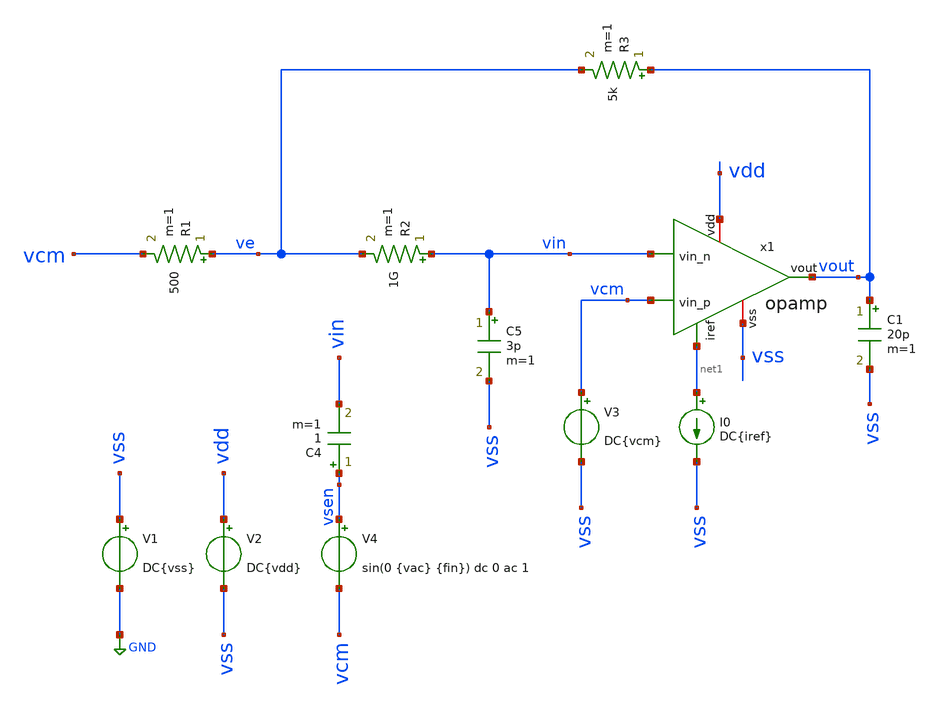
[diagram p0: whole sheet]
** sch_path: tb_opamp_openloop.sch
**.subckt tb_opamp_openloop
V1 vss GND DC{vss}
V2 vdd vss DC{vdd}
V3 vcm vss DC{vcm}
V4 vsen vcm sin(0 {vac} {fin}) dc 0 ac 1
C4 vsen vin 1 m=1
I0 net1 vss DC{iref}
R1 ve vcm 500 m=1
R2 vin ve 1G m=1
R3 vout ve 5k m=1
C5 vin vss 3p m=1
C1 vout vss 20p m=1
x1 vdd net1 vin vcm vout vss opamp
**** begin user architecture code




* Circuit Parameters

.param w_mirror_1 = 65
.param l_mirror_1 = 0.6
.param m_mirror_1 = 10

.param w_par = 41
.param l_par = 0.49
.param m_par = 48

.param w_mirror_2 = 40
.param l_mirror_2 = 1.4
.param m_mirror_2 = 8
.param cc = 13.25p

.param branch_2 = 20

.param iref = 100u
.param vdd  = 1.8
.param vss  = 0.0
.param vcm  = 0.8
.param vac  = 60m
.param fin  = 9.765625e5
.options TEMP = 65

* Include Models
.lib ~/skywater/skywater-pdk/libraries/sky130_fd_pr_ngspice/latest/models/corners/sky130.lib TT

* OP Parameters & Singals to save
.save all  @M.X1.XM1.msky130_fd_pr__pfet_01v8_lvt[id] @M.X1.XM1.msky130_fd_pr__pfet_01v8_lvt[vth] @M.X1.XM1.msky130_fd_pr__pfet_01v8_lvt[vgs] @M.X1.XM1.msky130_fd_pr__pfet_01v8_lvt[vds] @M.X1.XM1.msky130_fd_pr__pfet_01v8_lvt[vdsat] @M.X1.XM1.msky130_fd_pr__pfet_01v8_lvt[gm] @M.X1.XM1.msky130_fd_pr__pfet_01v8_lvt[gds]  @M.X1.XM2.msky130_fd_pr__pfet_01v8_lvt[id] @M.X1.XM2.msky130_fd_pr__pfet_01v8_lvt[vth] @M.X1.XM2.msky130_fd_pr__pfet_01v8_lvt[vgs] @M.X1.XM2.msky130_fd_pr__pfet_01v8_lvt[vds] @M.X1.XM2.msky130_fd_pr__pfet_01v8_lvt[vdsat] @M.X1.XM2.msky130_fd_pr__pfet_01v8_lvt[gm] @M.X1.XM2.msky130_fd_pr__pfet_01v8_lvt[gds] @M.X1.XM2.msky130_fd_pr__pfet_01v8[cgg]  @M.X1.XM3.msky130_fd_pr__nfet_01v8[id] @M.X1.XM3.msky130_fd_pr__nfet_01v8[vth] @M.X1.XM3.msky130_fd_pr__nfet_01v8[vgs] @M.X1.XM3.msky130_fd_pr__nfet_01v8[vds] @M.X1.XM3.msky130_fd_pr__nfet_01v8[vdsat] @M.X1.XM3.msky130_fd_pr__nfet_01v8[gm] @M.X1.XM3.msky130_fd_pr__nfet_01v8[gds]  @M.X1.XM4.msky130_fd_pr__nfet_01v8[id] @M.X1.XM4.msky130_fd_pr__nfet_01v8[vth] @M.X1.XM4.msky130_fd_pr__nfet_01v8[vgs] @M.X1.XM4.msky130_fd_pr__nfet_01v8[vds] @M.X1.XM4.msky130_fd_pr__nfet_01v8[vdsat] @M.X1.XM4.msky130_fd_pr__nfet_01v8[gm] @M.X1.XM4.msky130_fd_pr__nfet_01v8[gds]  @M.X1.XM5.msky130_fd_pr__pfet_01v8[id] @M.X1.XM5.msky130_fd_pr__pfet_01v8[vth] @M.X1.XM5.msky130_fd_pr__pfet_01v8[vgs] @M.X1.XM5.msky130_fd_pr__pfet_01v8[vds] @M.X1.XM5.msky130_fd_pr__pfet_01v8[vdsat] @M.X1.XM5.msky130_fd_pr__pfet_01v8[gm] @M.X1.XM5.msky130_fd_pr__pfet_01v8[gds]  @M.X1.XM6.msky130_fd_pr__nfet_01v8[id] @M.X1.XM6.msky130_fd_pr__nfet_01v8[vth] @M.X1.XM6.msky130_fd_pr__nfet_01v8[vgs] @M.X1.XM6.msky130_fd_pr__nfet_01v8[vds] @M.X1.XM6.msky130_fd_pr__nfet_01v8[vdsat] @M.X1.XM6.msky130_fd_pr__nfet_01v8[gm] @M.X1.XM6.msky130_fd_pr__nfet_01v8[gds] @M.X1.XM6.msky130_fd_pr__nfet_01v8[cgs]  @M.X1.XM7.msky130_fd_pr__pfet_01v8[id] @M.X1.XM7.msky130_fd_pr__pfet_01v8[vth] @M.X1.XM7.msky130_fd_pr__pfet_01v8[vgs] @M.X1.XM7.msky130_fd_pr__pfet_01v8[vds] @M.X1.XM7.msky130_fd_pr__pfet_01v8[vdsat] @M.X1.XM7.msky130_fd_pr__pfet_01v8[gm] @M.X1.XM7.msky130_fd_pr__pfet_01v8[gds]  @M.X1.XM8.msky130_fd_pr__pfet_01v8[id] @M.X1.XM8.msky130_fd_pr__pfet_01v8[vth] @M.X1.XM8.msky130_fd_pr__pfet_01v8[vgs] @M.X1.XM8.msky130_fd_pr__pfet_01v8[vds] @M.X1.XM8.msky130_fd_pr__pfet_01v8[vdsat] @M.X1.XM8.msky130_fd_pr__pfet_01v8[gm] @M.X1.XM8.msky130_fd_pr__pfet_01v8[gds]  @M.X1.XM9.msky130_fd_pr__nfet_01v8[id] @M.X1.XM9.msky130_fd_pr__nfet_01v8[vth] @M.X1.XM9.msky130_fd_pr__nfet_01v8[vgs] @M.X1.XM9.msky130_fd_pr__nfet_01v8[vds] @M.X1.XM9.msky130_fd_pr__nfet_01v8[vdsat] @M.X1.XM9.msky130_fd_pr__nfet_01v8[gm] @M.X1.XM9.msky130_fd_pr__nfet_01v8[gds]

*Simulation
.control
  set color0 = white

  ac dec 100 1 10G
  setplot ac1
  meas ac GBW when vdb(vout)=0
  meas ac DCG find vdb(vout) at=1
  meas ac PM find vp(vout) when vdb(vout)=0
  print PM*180/PI
  meas ac GM find vdb(vout) when vp(vout)=0
  plot vdb(vout) {vp(vout)*180/PI}
  write tb_opamp_openloop_ac1.raw

  reset
  op
  setplot op1
  unset filetype
  write tb_opamp_openloop.raw
.endc

.end


**** end user architecture code
**.ends

* expanding   symbol:  opamp.sym # of pins=6
** sym_path: opamp.sym
** sch_path: opamp.sch
.subckt opamp vdd iref vin_n vin_p vout vss
*.iopin vdd
*.iopin vss
*.ipin vin_n
*.ipin vin_p
*.ipin iref
*.opin vout
XM3 vbn vbn vss vss sky130_fd_pr__nfet_01v8 L={l_mirror_2} W={w_mirror_2} nf=1 ad='W * 0.29' as='W * 0.29'
+ pd='2 * (W + 0.29)' ps='2 * (W + 0.29)' nrd='0.29 / W' nrs='0.29 / W' sa=0 sb=0 sd=0 mult={m_mirror_2}
+ m={m_mirror_2}
XM4 voe1 vbn vss vss sky130_fd_pr__nfet_01v8 L={l_mirror_2} W={w_mirror_2} nf=1 ad='W * 0.29' as='W * 0.29'
+ pd='2 * (W + 0.29)' ps='2 * (W + 0.29)' nrd='0.29 / W' nrs='0.29 / W' sa=0 sb=0 sd=0 mult={m_mirror_2}
+ m={m_mirror_2}
XM5 vp iref vdd vdd sky130_fd_pr__pfet_01v8 L={l_mirror_1} W={w_mirror_1} nf=1 ad='W * 0.29' as='W * 0.29'
+ pd='2 * (W + 0.29)' ps='2 * (W + 0.29)' nrd='0.29 / W' nrs='0.29 / W' sa=0 sb=0 sd=0 mult=12*10 m=12*10
XM7 vout iref vdd vdd sky130_fd_pr__pfet_01v8 L={l_mirror_1} W={w_mirror_1} nf=1 ad='W * 0.29' as='W * 0.29'
+ pd='2 * (W + 0.29)' ps='2 * (W + 0.29)' nrd='0.29 / W' nrs='0.29 / W' sa=0 sb=0 sd=0 mult=18*10 m=18*10
XM8 iref iref vdd vdd sky130_fd_pr__pfet_01v8 L={l_mirror_1} W={w_mirror_1} nf=1 ad='W * 0.29' as='W * 0.29'
+ pd='2 * (W + 0.29)' ps='2 * (W + 0.29)' nrd='0.29 / W' nrs='0.29 / W' sa=0 sb=0 sd=0 mult={m_mirror_1}
+ m={m_mirror_1}
XM9 net1 vdd voe1 vss sky130_fd_pr__nfet_01v8 L=0.15 W=20 nf=1 ad='W * 0.29' as='W * 0.29' pd='2 * (W + 0.29)'
+ ps='2 * (W + 0.29)' nrd='0.29 / W' nrs='0.29 / W' sa=0 sb=0 sd=0 mult=1 m=1
XM6 vout voe1 vss vss sky130_fd_pr__nfet_01v8 L=0.3 W=39.46 nf=1 ad='W * 0.29' as='W * 0.29' pd='2 * (W + 0.29)'
+ ps='2 * (W + 0.29)' nrd='0.29 / W' nrs='0.29 / W' sa=0 sb=0 sd=0 mult=17 m=17
XM1 vbn vin_n vp vp sky130_fd_pr__pfet_01v8_lvt L={l_par} W={w_par} nf=1 ad='int((nf+1)/2) * W/nf * 0.29'
+ as='int((nf+2)/2) * W/nf * 0.29' pd='2*int((nf+1)/2) * (W/nf + 0.29)' ps='2*int((nf+2)/2) * (W/nf + 0.29)'
+ nrd='0.29 / W' nrs='0.29 / W' sa=0 sb=0 sd=0 mult={m_par} m={m_par}
XM2 voe1 vin_p vp vp sky130_fd_pr__pfet_01v8_lvt L={l_par} W={w_par} nf=1 ad='int((nf+1)/2) * W/nf * 0.29'
+ as='int((nf+2)/2) * W/nf * 0.29' pd='2*int((nf+1)/2) * (W/nf + 0.29)' ps='2*int((nf+2)/2) * (W/nf + 0.29)'
+ nrd='0.29 / W' nrs='0.29 / W' sa=0 sb=0 sd=0 mult={m_par} m={m_par}
C1 net1 vout {cc} m=1
.ends

.GLOBAL GND
.end
